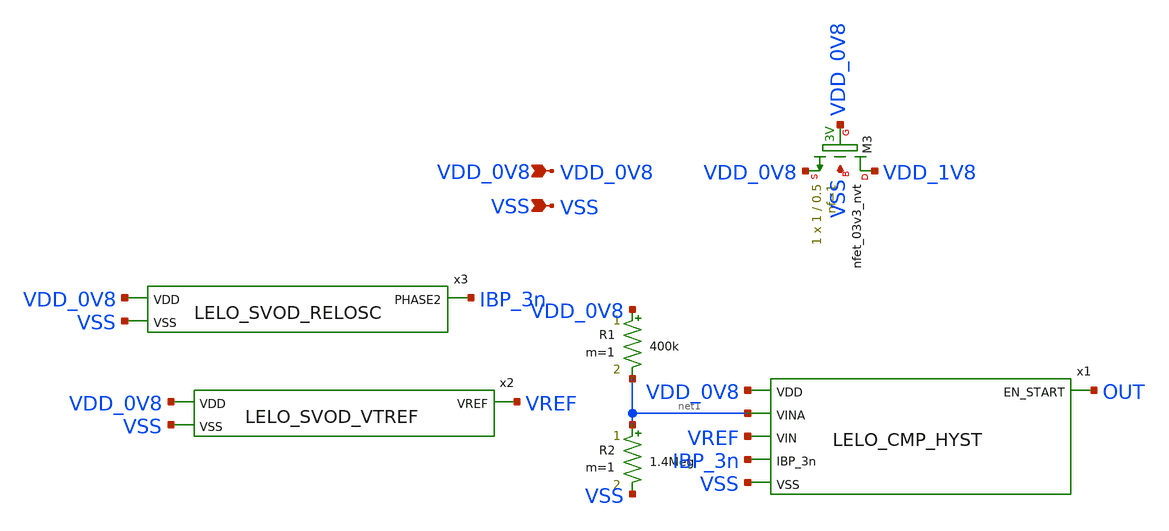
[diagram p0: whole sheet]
** sch_path: design/LELO_SVOD_SKY130A/LELO_STARTUP_DETECTOR_TEST.sch
**.subckt LELO_STARTUP_DETECTOR_TEST VDD_0V8 VSS
*.ipin VDD_0V8
*.ipin VSS
x1 VDD_0V8 OUT net1 VREF IBP_3n VSS LELO_CMP_HYST
x2 VDD_0V8 VSS VREF LELO_SVOD_VTREF
R1 VDD_0V8 net1 400k m=1
R2 net1 VSS 1.4Meg m=1
XM3 VDD_1V8 VDD_0V8 VDD_0V8 VSS sky130_fd_pr__nfet_03v3_nvt L=0.5 W=1 nf=1 ad='int((1 + 1)/2) * 1 / 1 * 0.29'
+ as='int((1 + 2)/2) * 1 / 1 * 0.29' pd='2*int((1 + 1)/2) * (1 / 1 + 0.29)' ps='2*int((1 + 2)/2) * (1 / 1 + 0.29)'
+ nrd='0.29 / 1 ' nrs='0.29 / 1 ' sa=0 sb=0 sd=0 mult=1 m=1
x3 VDD_0V8 VSS IBP_3n LELO_SVOD_RELOSC
**.ends
.end
